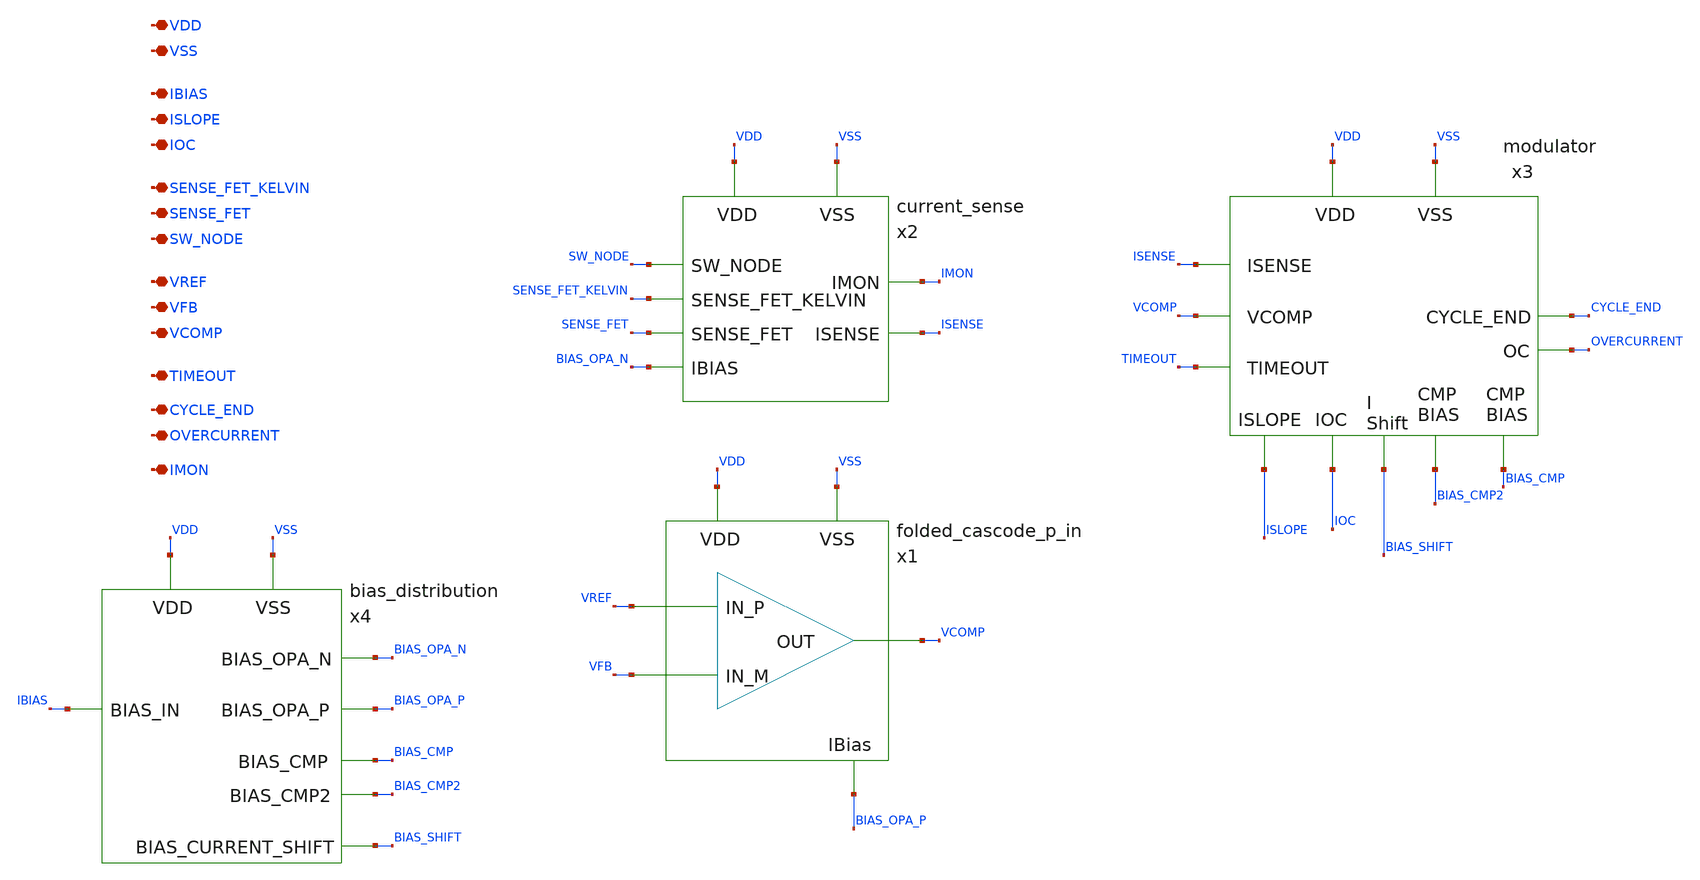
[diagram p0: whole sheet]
** sch_path: images/iic-osic-tools/addons/examples/open-pmic/design/system/analog_subsystem.sch
**.subckt analog_subsystem VDD VSS IBIAS SENSE_FET SW_NODE ISLOPE VREF VFB VCOMP TIMEOUT CYCLE_END
*+ IMON IOC OVERCURRENT SENSE_FET_KELVIN
*.iopin VDD
*.iopin VSS
*.iopin IBIAS
*.iopin SENSE_FET
*.iopin SW_NODE
*.iopin ISLOPE
*.iopin VREF
*.iopin VFB
*.iopin VCOMP
*.iopin TIMEOUT
*.iopin CYCLE_END
*.iopin IMON
*.iopin IOC
*.iopin OVERCURRENT
*.iopin SENSE_FET_KELVIN
x1 VREF VFB VCOMP VDD VSS BIAS_OPA_P folded_cascode_p_in
x2 VDD VSS SW_NODE SENSE_FET BIAS_OPA_N IMON ISENSE SENSE_FET_KELVIN current_sense
x3 VDD VSS BIAS_CMP ISLOPE ISENSE VCOMP TIMEOUT CYCLE_END BIAS_CMP2 IOC OVERCURRENT BIAS_SHIFT
+ modulator
x4 VDD VSS IBIAS BIAS_OPA_N BIAS_OPA_P BIAS_CMP BIAS_CMP2 BIAS_SHIFT bias_distribution
**.ends
.end
